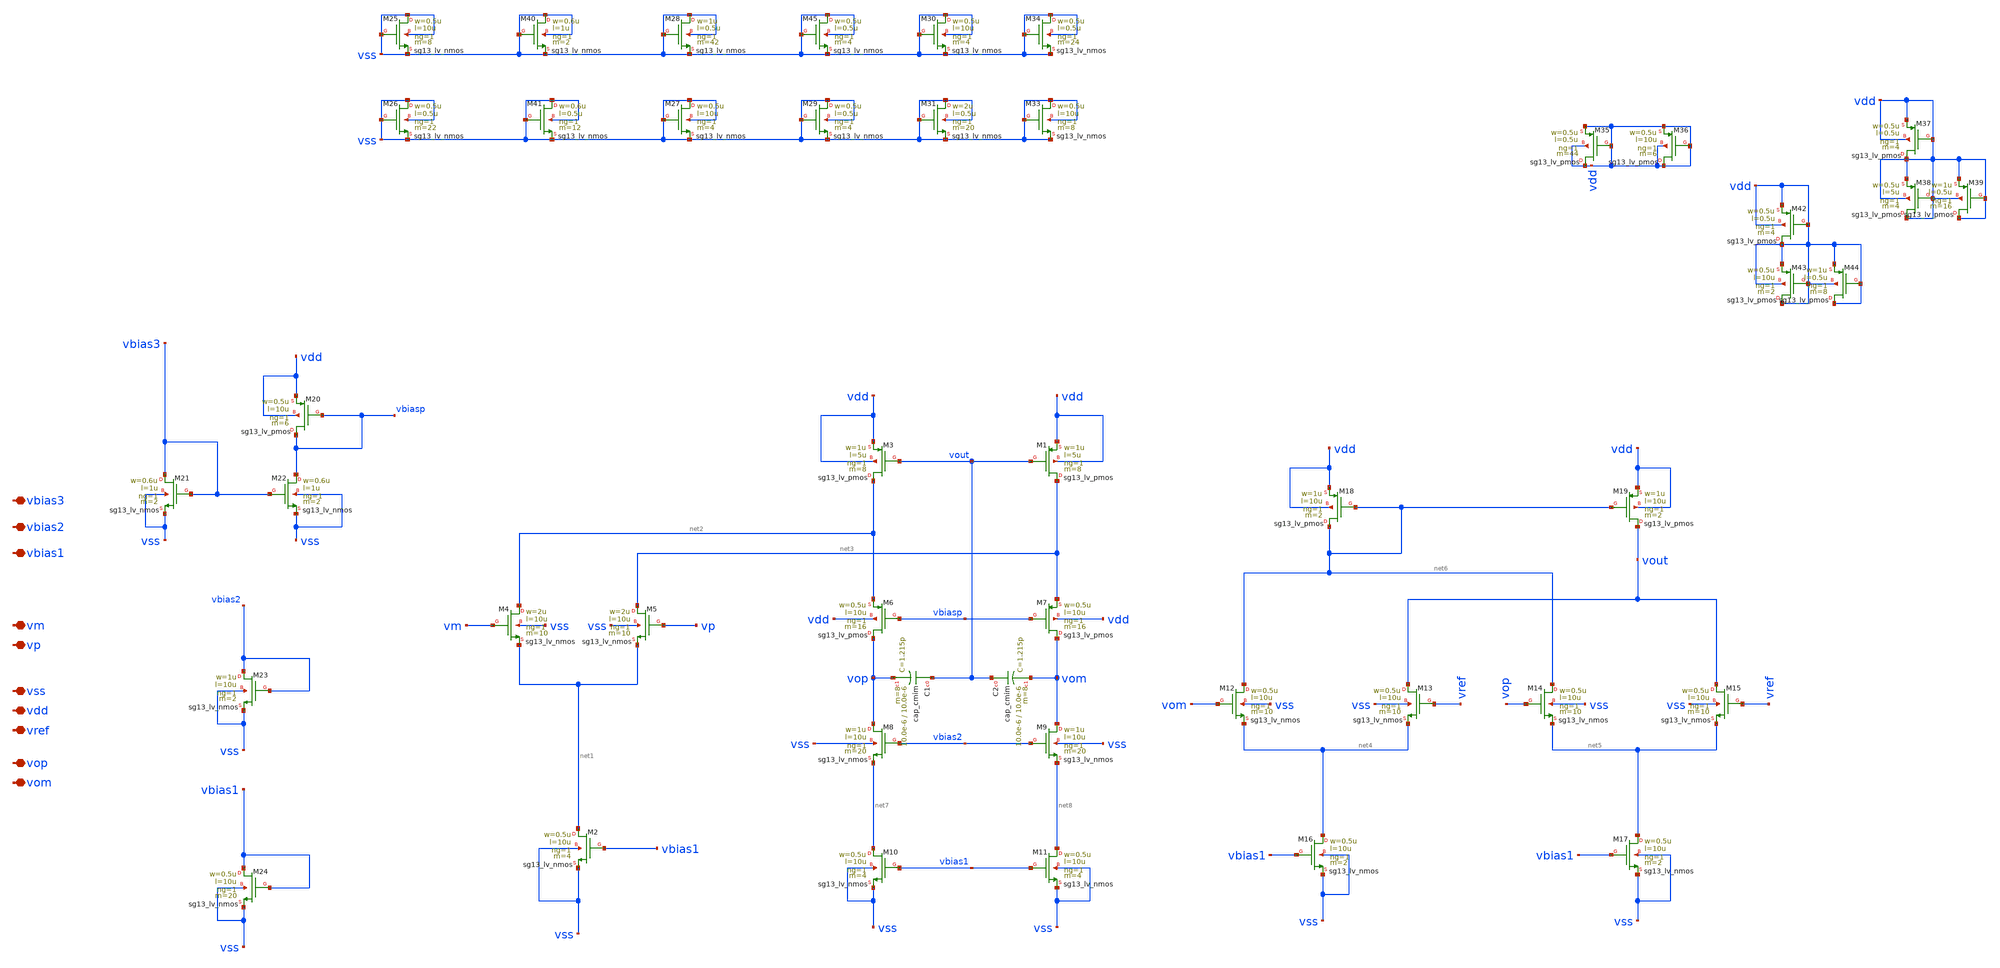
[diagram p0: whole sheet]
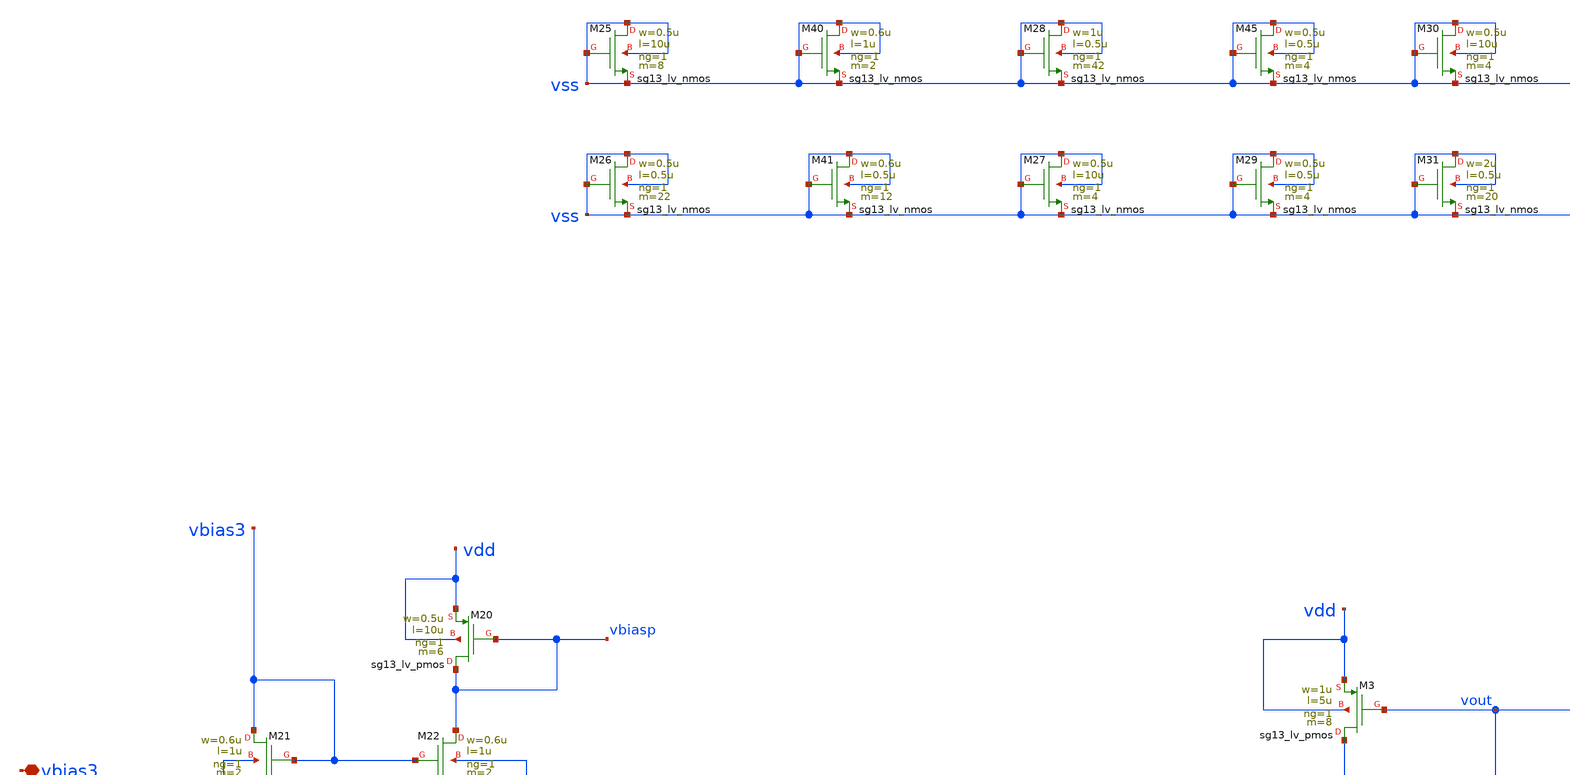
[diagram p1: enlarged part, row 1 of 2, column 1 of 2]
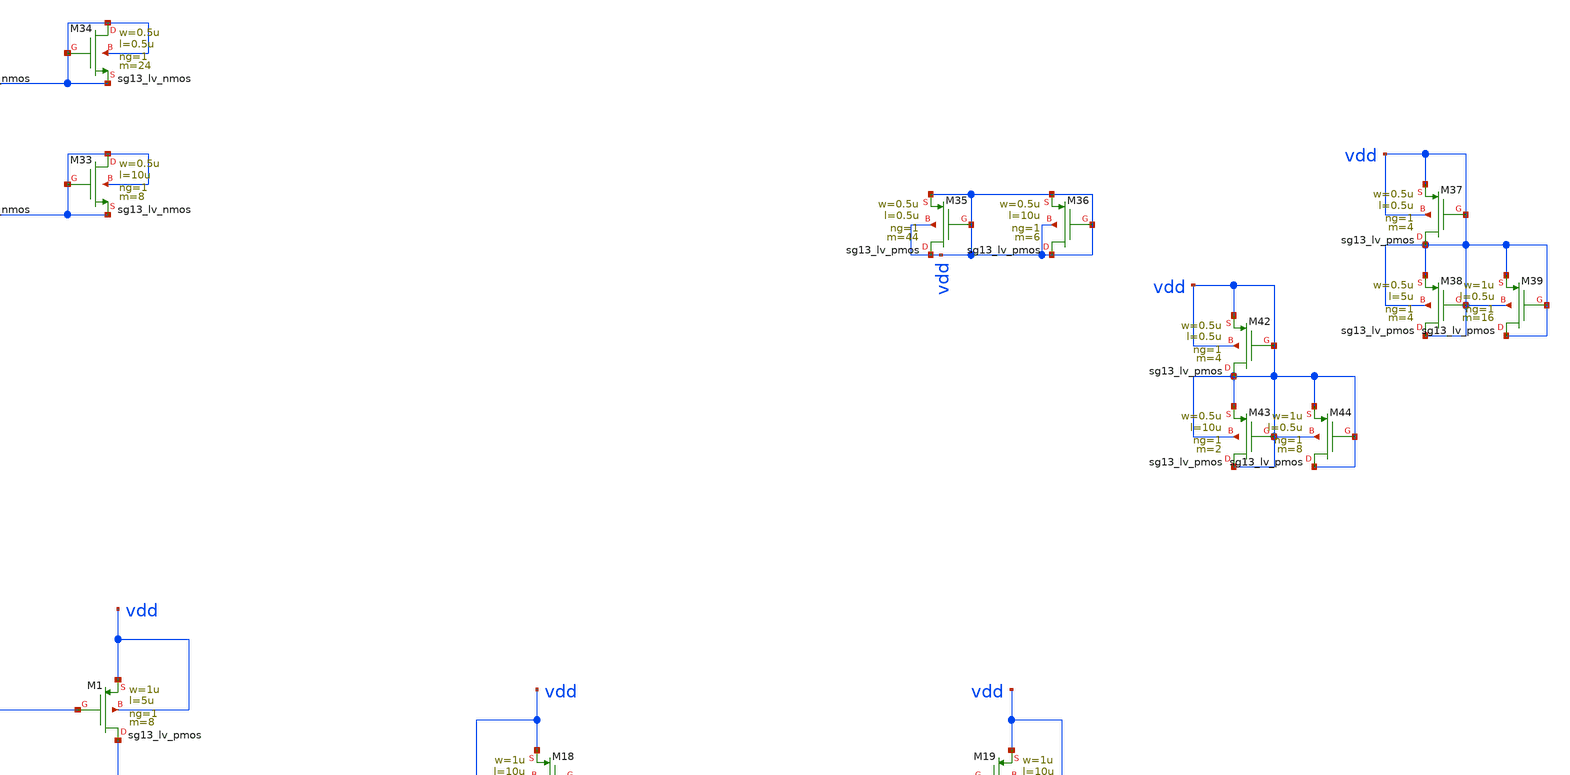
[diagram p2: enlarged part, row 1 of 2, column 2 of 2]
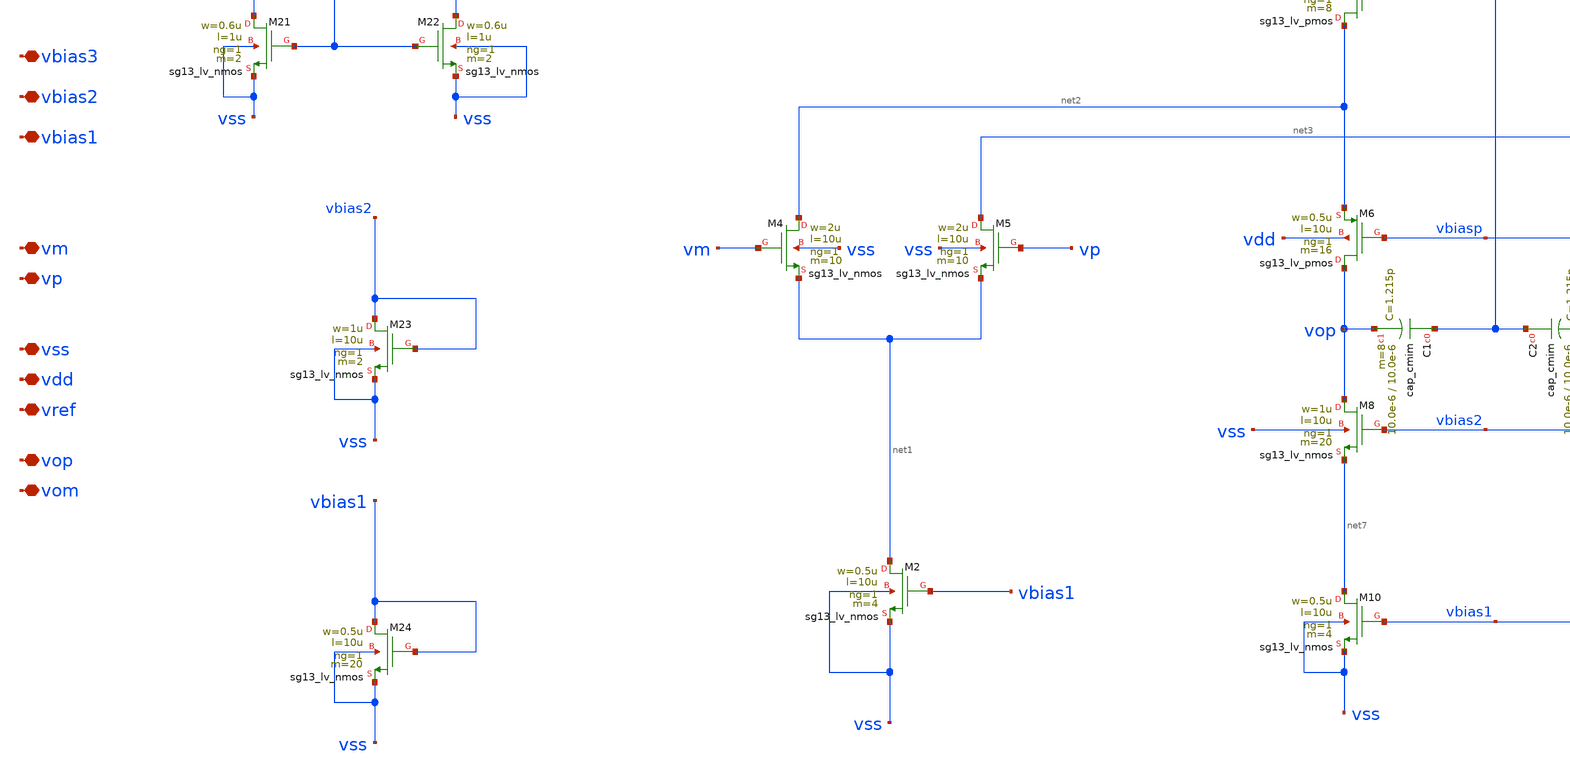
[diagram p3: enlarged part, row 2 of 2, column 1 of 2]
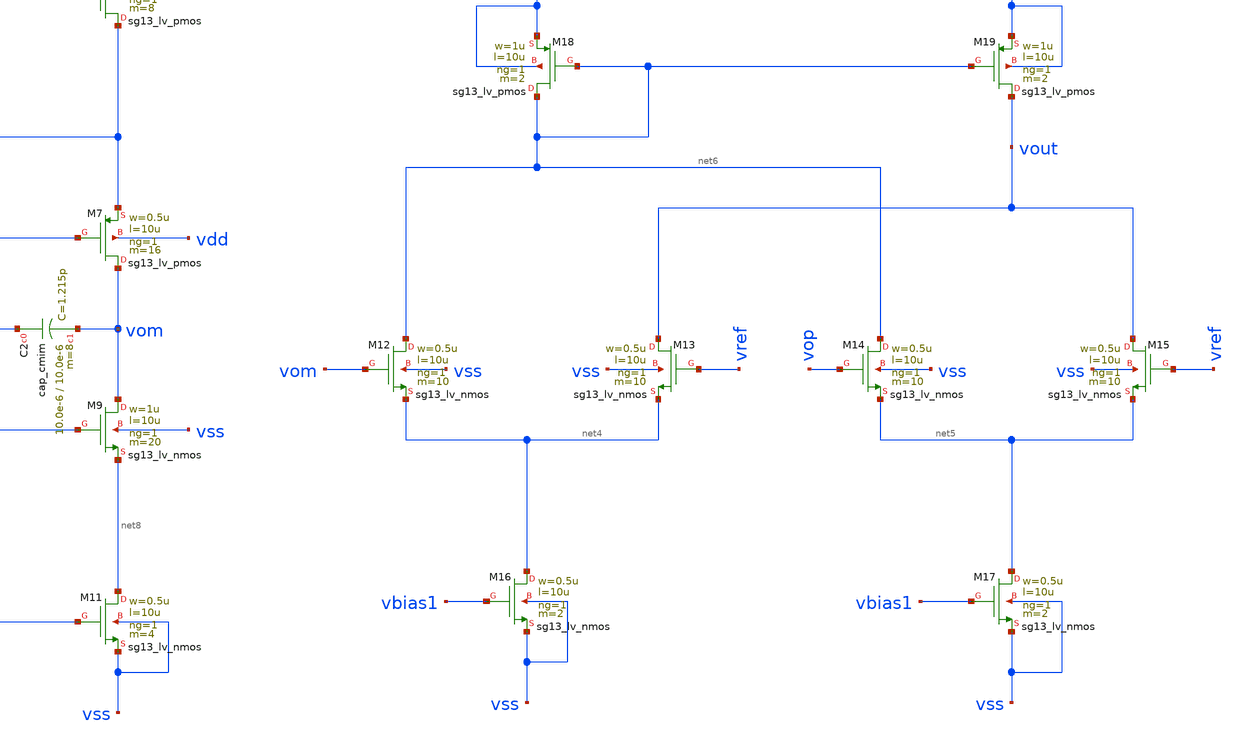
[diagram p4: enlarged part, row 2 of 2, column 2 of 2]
** sch_path: LVS/Unic_cass_final_design_lvs/Simulations/Opamp_design/Src/Folded_cascode.sch
**.subckt Folded_cascode vbias3 vbias2 vbias1 vm vp vss vdd vref vop vom
*.iopin vbias3
*.iopin vbias2
*.iopin vbias1
*.iopin vm
*.iopin vp
*.iopin vss
*.iopin vdd
*.iopin vref
*.iopin vop
*.iopin vom
XM1 net3 vout vdd vdd sg13_lv_pmos w=1u l=5u ng=1 m=8 mm_ok=1
XM2 net1 vbias1 vss vss sg13_lv_nmos w=0.5u l=10u ng=1 m=4 mm_ok=1
XM4 net2 vm net1 vss sg13_lv_nmos w=2u l=10u ng=1 m=10 mm_ok=1
XM5 net3 vp net1 vss sg13_lv_nmos w=2u l=10u ng=1 m=10 mm_ok=1
XM3 net2 vout vdd vdd sg13_lv_pmos w=1u l=5u ng=1 m=8 mm_ok=1
XM6 vop vbiasp net2 vdd sg13_lv_pmos w=0.5u l=10u ng=1 m=16 mm_ok=1
XM7 vom vbiasp net3 vdd sg13_lv_pmos w=0.5u l=10u ng=1 m=16 mm_ok=1
XM8 vop vbias2 net7 vss sg13_lv_nmos w=1u l=10u ng=1 m=20 mm_ok=1
XM9 vom vbias2 net8 vss sg13_lv_nmos w=1u l=10u ng=1 m=20 mm_ok=1
XM10 net7 vbias1 vss vss sg13_lv_nmos w=0.5u l=10u ng=1 m=4 mm_ok=1
XM11 net8 vbias1 vss vss sg13_lv_nmos w=0.5u l=10u ng=1 m=4 mm_ok=1
XM12 net6 vom net4 vss sg13_lv_nmos w=0.5u l=10u ng=1 m=10 mm_ok=1
XM13 vout vref net4 vss sg13_lv_nmos w=0.5u l=10u ng=1 m=10 mm_ok=1
XM14 net6 vop net5 vss sg13_lv_nmos w=0.5u l=10u ng=1 m=10 mm_ok=1
XM15 vout vref net5 vss sg13_lv_nmos w=0.5u l=10u ng=1 m=10 mm_ok=1
XM16 net4 vbias1 vss vss sg13_lv_nmos w=0.5u l=10u ng=1 m=2 mm_ok=1
XM17 net5 vbias1 vss vss sg13_lv_nmos w=0.5u l=10u ng=1 m=2 mm_ok=1
XM18 net6 net6 vdd vdd sg13_lv_pmos w=1u l=10u ng=1 m=2 mm_ok=1
XM19 vout net6 vdd vdd sg13_lv_pmos w=1u l=10u ng=1 m=2 mm_ok=1
XM20 vbiasp vbiasp vdd vdd sg13_lv_pmos w=0.5u l=10u ng=1 m=6 mm_ok=1
XM21 vbias3 vbias3 vss vss sg13_lv_nmos w=0.6u l=1u ng=1 m=2 mm_ok=1
XM22 vbiasp vbias3 vss vss sg13_lv_nmos w=0.6u l=1u ng=1 m=2 mm_ok=1
XM23 vbias2 vbias2 vss vss sg13_lv_nmos w=1u l=10u ng=1 m=2 mm_ok=1
XM24 vbias1 vbias1 vss vss sg13_lv_nmos w=0.5u l=10u ng=1 m=20 mm_ok=1
XC1 vout vop cap_cmim w=10.0e-6 l=10.0e-6 m=8 mm_ok=1
XC2 vout vom cap_cmim w=10.0e-6 l=10.0e-6 m=8 mm_ok=1
XM25 vss vss vss vss sg13_lv_nmos w=0.5u l=10u ng=1 m=8 mm_ok=1
XM26 vss vss vss vss sg13_lv_nmos w=0.5u l=0.5u ng=1 m=22 mm_ok=1
XM27 vss vss vss vss sg13_lv_nmos w=0.5u l=10u ng=1 m=4 mm_ok=1
XM28 vss vss vss vss sg13_lv_nmos w=1u l=0.5u ng=1 m=42 mm_ok=1
XM29 vss vss vss vss sg13_lv_nmos w=0.5u l=0.5u ng=1 m=4 mm_ok=1
XM30 vss vss vss vss sg13_lv_nmos w=0.5u l=10u ng=1 m=4 mm_ok=1
XM31 vss vss vss vss sg13_lv_nmos w=2u l=0.5u ng=1 m=20 mm_ok=1
XM33 vss vss vss vss sg13_lv_nmos w=0.5u l=10u ng=1 m=8 mm_ok=1
XM34 vss vss vss vss sg13_lv_nmos w=0.5u l=0.5u ng=1 m=24 mm_ok=1
XM35 vdd vdd vdd vdd sg13_lv_pmos w=0.5u l=0.5u ng=1 m=44 mm_ok=1
XM36 vdd vdd vdd vdd sg13_lv_pmos w=0.5u l=10u ng=1 m=6 mm_ok=1
XM37 vdd vdd vdd vdd sg13_lv_pmos w=0.5u l=0.5u ng=1 m=4 mm_ok=1
XM38 vdd vdd vdd vdd sg13_lv_pmos w=0.5u l=5u ng=1 m=4 mm_ok=1
XM39 vdd vdd vdd vdd sg13_lv_pmos w=1u l=0.5u ng=1 m=16 mm_ok=1
XM40 vss vss vss vss sg13_lv_nmos w=0.6u l=1u ng=1 m=2 mm_ok=1
XM41 vss vss vss vss sg13_lv_nmos w=0.6u l=0.5u ng=1 m=12 mm_ok=1
XM42 vdd vdd vdd vdd sg13_lv_pmos w=0.5u l=0.5u ng=1 m=4 mm_ok=1
XM43 vdd vdd vdd vdd sg13_lv_pmos w=0.5u l=10u ng=1 m=2 mm_ok=1
XM44 vdd vdd vdd vdd sg13_lv_pmos w=1u l=0.5u ng=1 m=8 mm_ok=1
XM45 vss vss vss vss sg13_lv_nmos w=0.5u l=0.5u ng=1 m=4 mm_ok=1
**.ends
.end
